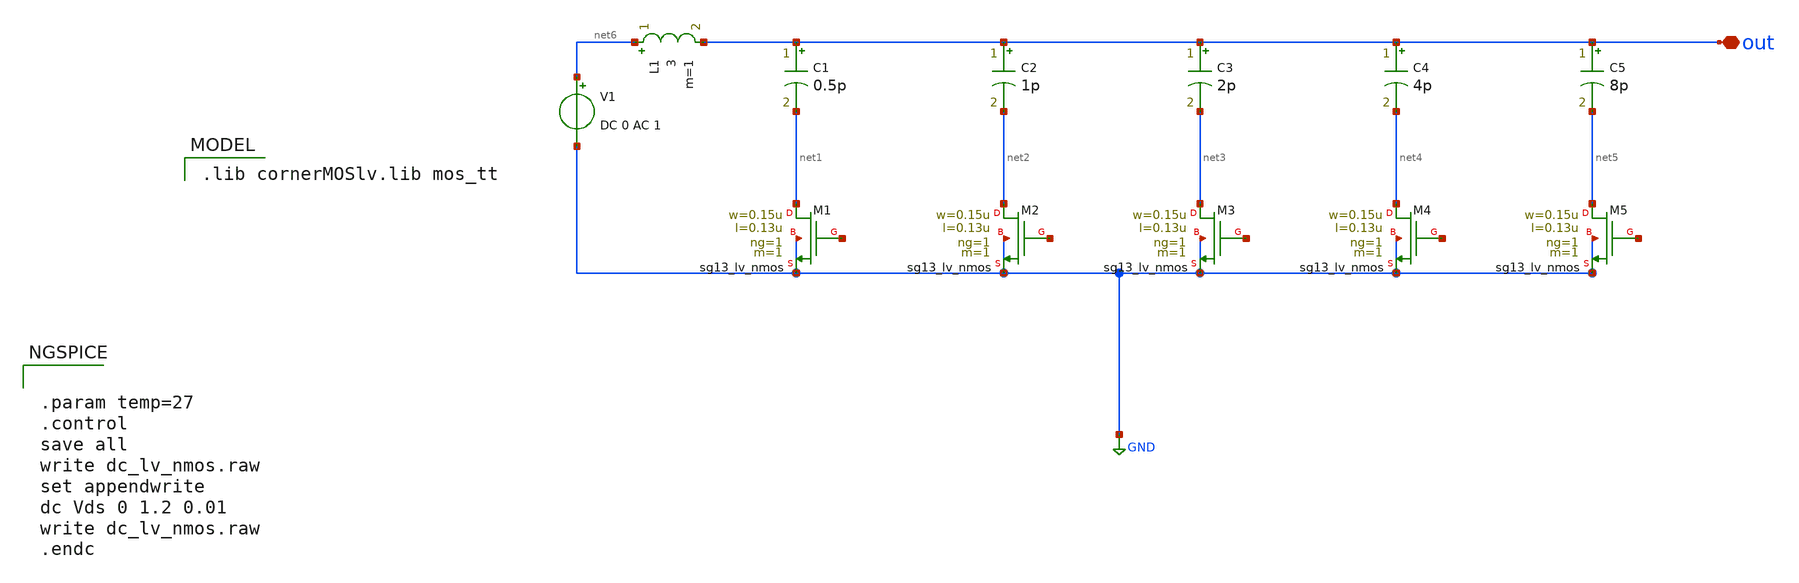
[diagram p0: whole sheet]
** sch_path: xschem/phs01.sch
**.subckt phs01 out
*.iopin out
L1 net6 out 3 m=1
C1 out net1 0.5p m=1
XM1 net1 net7 GND GND sg13_lv_nmos w=0.15u l=0.13u ng=1 m=1 mm_ok=1
C2 out net2 1p m=1
XM2 net2 net8 GND GND sg13_lv_nmos w=0.15u l=0.13u ng=1 m=1 mm_ok=1
C3 out net3 2p m=1
XM3 net3 net9 GND GND sg13_lv_nmos w=0.15u l=0.13u ng=1 m=1 mm_ok=1
C4 out net4 4p m=1
XM4 net4 net10 GND GND sg13_lv_nmos w=0.15u l=0.13u ng=1 m=1 mm_ok=1
C5 out net5 8p m=1
XM5 net5 net11 GND GND sg13_lv_nmos w=0.15u l=0.13u ng=1 m=1 mm_ok=1
V1 net6 GND DC 0 AC 1
**** begin user architecture code
 .lib cornerMOSlv.lib mos_tt



.param temp=27
.control
save all
write dc_lv_nmos.raw
set appendwrite
dc Vds 0 1.2 0.01
write dc_lv_nmos.raw
.endc


**** end user architecture code
**.ends
.GLOBAL GND
.end
